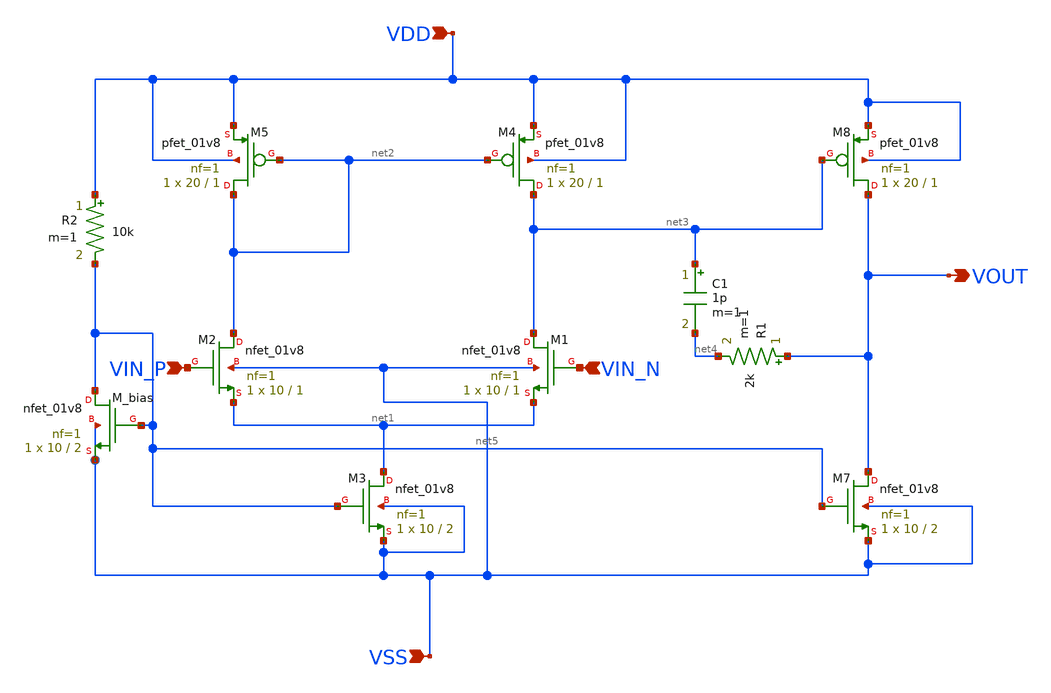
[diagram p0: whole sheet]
** sch_path: analog/build/schematic/opamp_two_stage.sch
**.subckt opamp_two_stage VIN_N VIN_P VOUT VDD VSS
*.ipin VIN_N
*.ipin VIN_P
*.opin VOUT
*.ipin VDD
*.ipin VSS
XM1 net3 VIN_N net1 VSS sky130_fd_pr__nfet_01v8 L=1 W=10 nf=1 ad='int((nf+1)/2) * W/nf * 0.29' as='int((nf+2)/2) * W/nf * 0.29'
+ pd='2*int((nf+1)/2) * (W/nf + 0.29)' ps='2*int((nf+2)/2) * (W/nf + 0.29)' nrd='0.29 / W' nrs='0.29 / W'
+ sa=0 sb=0 sd=0 mult=1 m=1
XM2 net2 VIN_P net1 VSS sky130_fd_pr__nfet_01v8 L=1 W=10 nf=1 ad='int((nf+1)/2) * W/nf * 0.29' as='int((nf+2)/2) * W/nf * 0.29'
+ pd='2*int((nf+1)/2) * (W/nf + 0.29)' ps='2*int((nf+2)/2) * (W/nf + 0.29)' nrd='0.29 / W' nrs='0.29 / W'
+ sa=0 sb=0 sd=0 mult=1 m=1
XM3 net1 net5 VSS VSS sky130_fd_pr__nfet_01v8 L=2 W=10 nf=1 ad='int((nf+1)/2) * W/nf * 0.29' as='int((nf+2)/2) * W/nf * 0.29'
+ pd='2*int((nf+1)/2) * (W/nf + 0.29)' ps='2*int((nf+2)/2) * (W/nf + 0.29)' nrd='0.29 / W' nrs='0.29 / W'
+ sa=0 sb=0 sd=0 mult=1 m=1
XM4 net3 net2 VDD VDD sky130_fd_pr__pfet_01v8 L=1 W=20 nf=1 ad='int((nf+1)/2) * W/nf * 0.29' as='int((nf+2)/2) * W/nf * 0.29'
+ pd='2*int((nf+1)/2) * (W/nf + 0.29)' ps='2*int((nf+2)/2) * (W/nf + 0.29)' nrd='0.29 / W' nrs='0.29 / W'
+ sa=0 sb=0 sd=0 mult=1 m=1
XM5 net2 net2 VDD VDD sky130_fd_pr__pfet_01v8 L=1 W=20 nf=1 ad='int((nf+1)/2) * W/nf * 0.29' as='int((nf+2)/2) * W/nf * 0.29'
+ pd='2*int((nf+1)/2) * (W/nf + 0.29)' ps='2*int((nf+2)/2) * (W/nf + 0.29)' nrd='0.29 / W' nrs='0.29 / W'
+ sa=0 sb=0 sd=0 mult=1 m=1
XM7 VOUT net5 VSS VSS sky130_fd_pr__nfet_01v8 L=2 W=10 nf=1 ad='int((nf+1)/2) * W/nf * 0.29' as='int((nf+2)/2) * W/nf * 0.29'
+ pd='2*int((nf+1)/2) * (W/nf + 0.29)' ps='2*int((nf+2)/2) * (W/nf + 0.29)' nrd='0.29 / W' nrs='0.29 / W'
+ sa=0 sb=0 sd=0 mult=1 m=1
XM8 VOUT net3 VDD VDD sky130_fd_pr__pfet_01v8 L=1 W=20 nf=1 ad='int((nf+1)/2) * W/nf * 0.29' as='int((nf+2)/2) * W/nf * 0.29'
+ pd='2*int((nf+1)/2) * (W/nf + 0.29)' ps='2*int((nf+2)/2) * (W/nf + 0.29)' nrd='0.29 / W' nrs='0.29 / W'
+ sa=0 sb=0 sd=0 mult=1 m=1
C1 net3 net4 1p m=1
R1 VOUT net4 2k m=1
XM_bias net5 net5 VSS VSS sky130_fd_pr__nfet_01v8 L=2 W=10 nf=1 ad='int((nf+1)/2) * W/nf * 0.29' as='int((nf+2)/2) * W/nf * 0.29'
+ pd='2*int((nf+1)/2) * (W/nf + 0.29)' ps='2*int((nf+2)/2) * (W/nf + 0.29)' nrd='0.29 / W' nrs='0.29 / W'
+ sa=0 sb=0 sd=0 mult=1 m=1
R2 VDD net5 10k m=1
**.ends
.end
